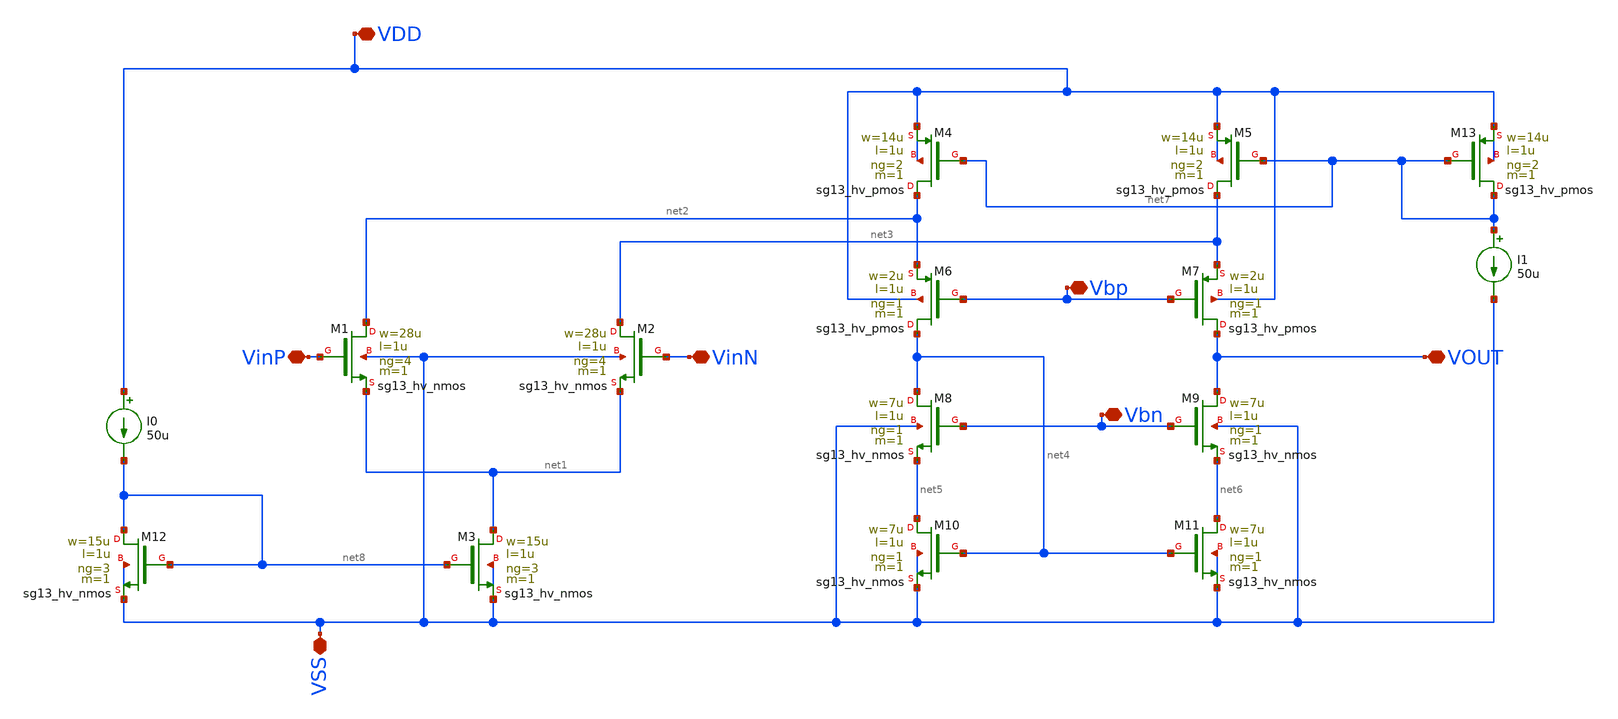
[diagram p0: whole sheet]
** sch_path: v1_ideal_current_sources/schematic/foldedOTA.sch
* (c) 2026 Fares Satouh
**.subckt foldedOTA VDD VSS VOUT Vbp Vbn VinN VinP
*.iopin VDD
*.iopin VSS
*.iopin VOUT
*.iopin Vbp
*.iopin Vbn
*.iopin VinN
*.iopin VinP
XM1 net2 VinP net1 VSS sg13_hv_nmos w=28u l=1u ng=4 m=1 mm_ok=1
XM2 net3 VinN net1 VSS sg13_hv_nmos w=28u l=1u ng=4 m=1 mm_ok=1
XM3 net1 net8 VSS VSS sg13_hv_nmos w=15u l=1u ng=3 m=1 mm_ok=1
XM4 net2 net7 VDD VDD sg13_hv_pmos w=14u l=1u ng=2 m=1 mm_ok=1
XM5 net3 net7 VDD VDD sg13_hv_pmos w=14u l=1u ng=2 m=1 mm_ok=1
XM6 net4 Vbp net2 VDD sg13_hv_pmos w=2u l=1u ng=1 m=1 mm_ok=1
XM7 VOUT Vbp net3 VDD sg13_hv_pmos w=2u l=1u ng=1 m=1 mm_ok=1
XM8 net4 Vbn net5 VSS sg13_hv_nmos w=7u l=1u ng=1 m=1 mm_ok=1
XM9 VOUT Vbn net6 VSS sg13_hv_nmos w=7u l=1u ng=1 m=1 mm_ok=1
XM10 net5 net4 VSS VSS sg13_hv_nmos w=7u l=1u ng=1 m=1 mm_ok=1
XM11 net6 net4 VSS VSS sg13_hv_nmos w=7u l=1u ng=1 m=1 mm_ok=1
XM12 net8 net8 VSS VSS sg13_hv_nmos w=15u l=1u ng=3 m=1 mm_ok=1
I0 VDD net8 50u
XM13 net7 net7 VDD VDD sg13_hv_pmos w=14u l=1u ng=2 m=1 mm_ok=1
I1 net7 VSS 50u
**.ends
.end
